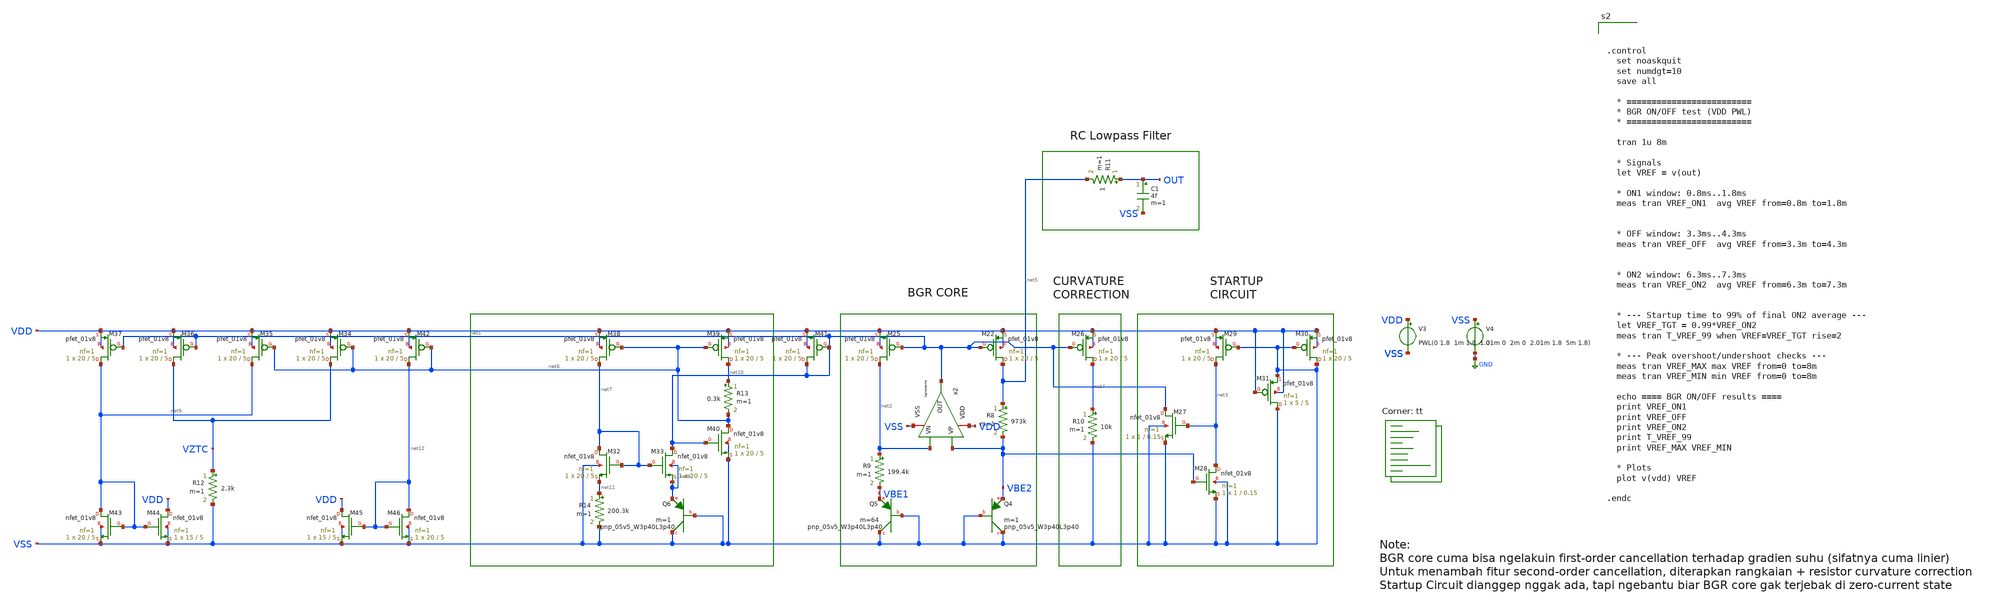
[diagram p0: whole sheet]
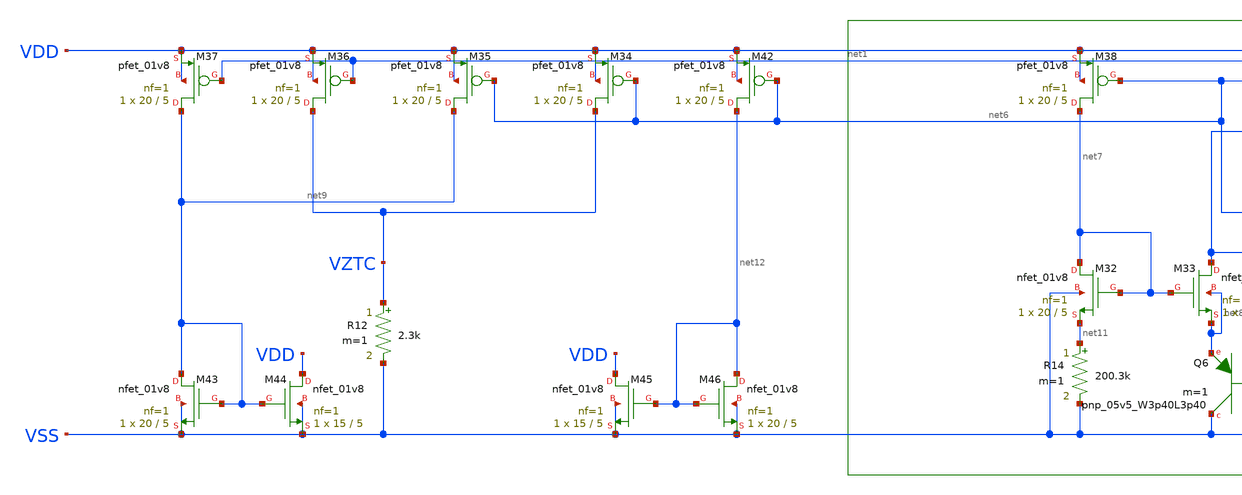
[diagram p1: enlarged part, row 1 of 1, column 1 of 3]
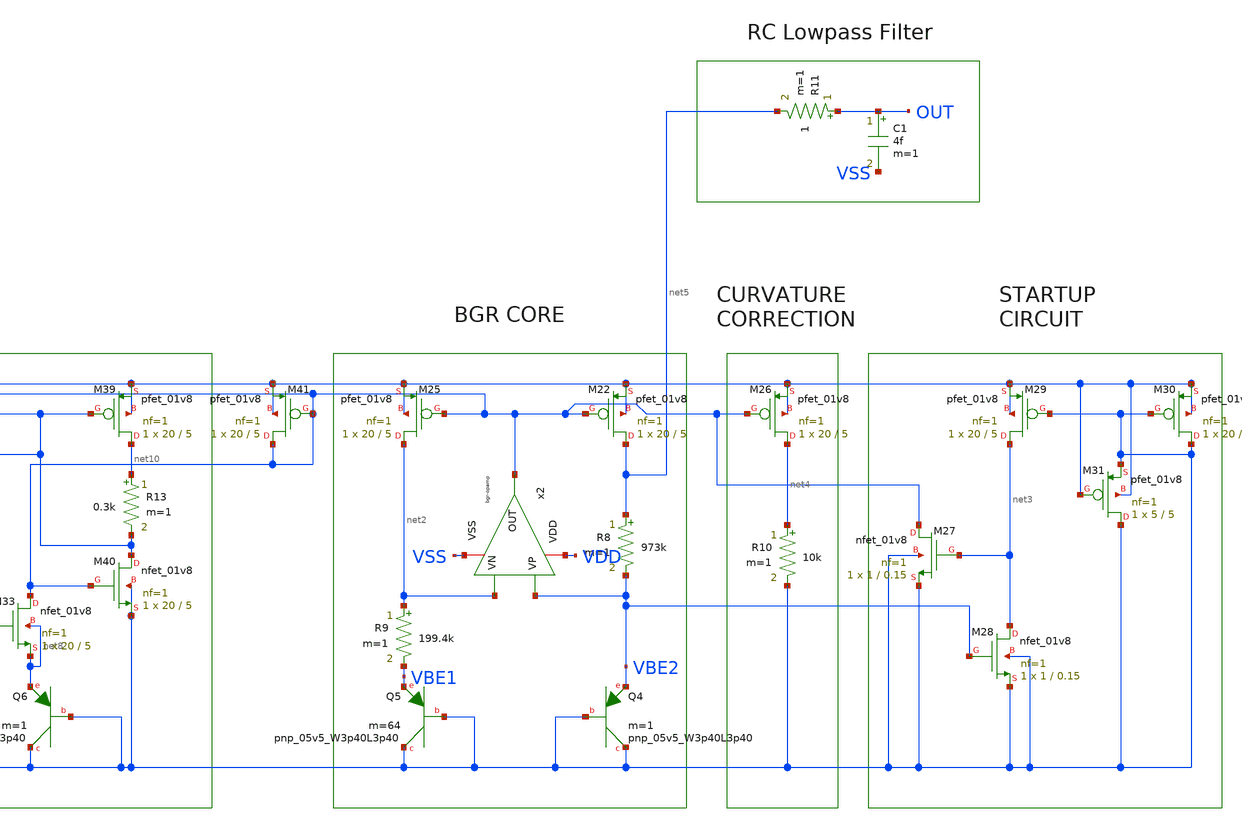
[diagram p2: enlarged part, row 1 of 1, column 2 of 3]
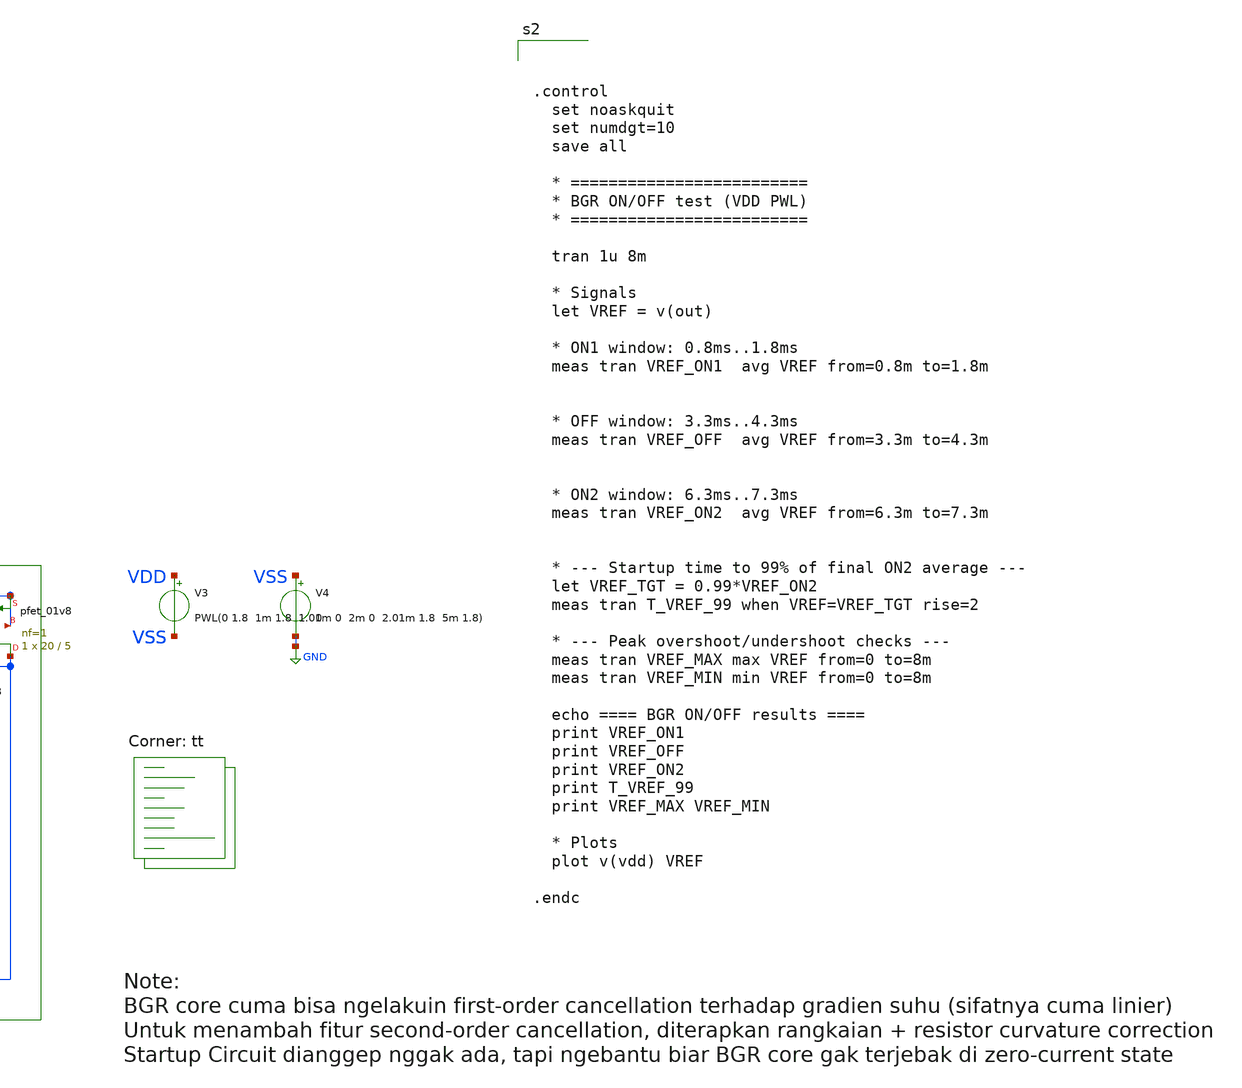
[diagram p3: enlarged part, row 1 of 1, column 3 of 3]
** sch_path: bandgap/bgr-final/tb_bgr-on-off.sch
**.subckt tb_bgr-on-off
V3 VDD VSS PWL(0 1.8 1m 1.8 1.01m 0 2m 0 2.01m 1.8 5m 1.8)
V4 VSS GND 0
x2 VDD net1 VBE2 net2 VSS bgr-opamp
XM22 net5 net1 VDD VDD sky130_fd_pr__pfet_01v8 L=5 W=20 nf=1 ad='int((nf+1)/2) * W/nf * 0.29' as='int((nf+2)/2) * W/nf * 0.29'
+ pd='2*int((nf+1)/2) * (W/nf + 0.29)' ps='2*int((nf+2)/2) * (W/nf + 0.29)' nrd='0.29 / W' nrs='0.29 / W'
+ sa=0 sb=0 sd=0 mult=1 m=1
XM25 net2 net1 VDD VDD sky130_fd_pr__pfet_01v8 L=5 W=20 nf=1 ad='int((nf+1)/2) * W/nf * 0.29' as='int((nf+2)/2) * W/nf * 0.29'
+ pd='2*int((nf+1)/2) * (W/nf + 0.29)' ps='2*int((nf+2)/2) * (W/nf + 0.29)' nrd='0.29 / W' nrs='0.29 / W'
+ sa=0 sb=0 sd=0 mult=1 m=1
R8 net5 VBE2 973k m=1
R9 net2 VBE1 199.4k m=1
XQ4 VSS VSS VBE2 sky130_fd_pr__pnp_05v5_W3p40L3p40 m=1
XQ5 VSS VSS VBE1 sky130_fd_pr__pnp_05v5_W3p40L3p40 m=64
XM26 net4 net1 VDD VDD sky130_fd_pr__pfet_01v8 L=5 W=20 nf=1 ad='int((nf+1)/2) * W/nf * 0.29' as='int((nf+2)/2) * W/nf * 0.29'
+ pd='2*int((nf+1)/2) * (W/nf + 0.29)' ps='2*int((nf+2)/2) * (W/nf + 0.29)' nrd='0.29 / W' nrs='0.29 / W'
+ sa=0 sb=0 sd=0 mult=1 m=1
R10 net4 VSS 10k m=1
XM27 net1 net3 VSS VSS sky130_fd_pr__nfet_01v8 L=0.15 W=1 nf=1 ad='int((nf+1)/2) * W/nf * 0.29' as='int((nf+2)/2) * W/nf * 0.29'
+ pd='2*int((nf+1)/2) * (W/nf + 0.29)' ps='2*int((nf+2)/2) * (W/nf + 0.29)' nrd='0.29 / W' nrs='0.29 / W'
+ sa=0 sb=0 sd=0 mult=1 m=1
XM28 net3 VBE2 VSS VSS sky130_fd_pr__nfet_01v8 L=0.15 W=1 nf=1 ad='int((nf+1)/2) * W/nf * 0.29' as='int((nf+2)/2) * W/nf * 0.29'
+ pd='2*int((nf+1)/2) * (W/nf + 0.29)' ps='2*int((nf+2)/2) * (W/nf + 0.29)' nrd='0.29 / W' nrs='0.29 / W'
+ sa=0 sb=0 sd=0 mult=1 m=1
XM29 net3 VSS VDD VDD sky130_fd_pr__pfet_01v8 L=5 W=20 nf=1 ad='int((nf+1)/2) * W/nf * 0.29' as='int((nf+2)/2) * W/nf * 0.29'
+ pd='2*int((nf+1)/2) * (W/nf + 0.29)' ps='2*int((nf+2)/2) * (W/nf + 0.29)' nrd='0.29 / W' nrs='0.29 / W'
+ sa=0 sb=0 sd=0 mult=1 m=1
XM30 VSS VSS VDD VDD sky130_fd_pr__pfet_01v8 L=5 W=20 nf=1 ad='int((nf+1)/2) * W/nf * 0.29' as='int((nf+2)/2) * W/nf * 0.29'
+ pd='2*int((nf+1)/2) * (W/nf + 0.29)' ps='2*int((nf+2)/2) * (W/nf + 0.29)' nrd='0.29 / W' nrs='0.29 / W'
+ sa=0 sb=0 sd=0 mult=1 m=1
XM31 VSS VDD VSS VDD sky130_fd_pr__pfet_01v8 L=5 W=5 nf=1 ad='int((nf+1)/2) * W/nf * 0.29' as='int((nf+2)/2) * W/nf * 0.29'
+ pd='2*int((nf+1)/2) * (W/nf + 0.29)' ps='2*int((nf+2)/2) * (W/nf + 0.29)' nrd='0.29 / W' nrs='0.29 / W'
+ sa=0 sb=0 sd=0 mult=1 m=1
C1 OUT VSS 4f m=1
R11 OUT net5 1 m=1
XM32 net7 net7 net11 VSS sky130_fd_pr__nfet_01v8 L=5 W=20 nf=1 ad='int((nf+1)/2) * W/nf * 0.29' as='int((nf+2)/2) * W/nf * 0.29'
+ pd='2*int((nf+1)/2) * (W/nf + 0.29)' ps='2*int((nf+2)/2) * (W/nf + 0.29)' nrd='0.29 / W' nrs='0.29 / W'
+ sa=0 sb=0 sd=0 mult=1 m=1
XM33 net1 net7 net8 net8 sky130_fd_pr__nfet_01v8 L=5 W=20 nf=1 ad='int((nf+1)/2) * W/nf * 0.29' as='int((nf+2)/2) * W/nf * 0.29'
+ pd='2*int((nf+1)/2) * (W/nf + 0.29)' ps='2*int((nf+2)/2) * (W/nf + 0.29)' nrd='0.29 / W' nrs='0.29 / W'
+ sa=0 sb=0 sd=0 mult=1 m=1
XQ6 VSS VSS net8 sky130_fd_pr__pnp_05v5_W3p40L3p40 m=1
XM34 VZTC net6 VDD VDD sky130_fd_pr__pfet_01v8 L=5 W=20 nf=1 ad='int((nf+1)/2) * W/nf * 0.29' as='int((nf+2)/2) * W/nf * 0.29'
+ pd='2*int((nf+1)/2) * (W/nf + 0.29)' ps='2*int((nf+2)/2) * (W/nf + 0.29)' nrd='0.29 / W' nrs='0.29 / W'
+ sa=0 sb=0 sd=0 mult=1 m=1
XM35 net9 net6 VDD VDD sky130_fd_pr__pfet_01v8 L=5 W=20 nf=1 ad='int((nf+1)/2) * W/nf * 0.29' as='int((nf+2)/2) * W/nf * 0.29'
+ pd='2*int((nf+1)/2) * (W/nf + 0.29)' ps='2*int((nf+2)/2) * (W/nf + 0.29)' nrd='0.29 / W' nrs='0.29 / W'
+ sa=0 sb=0 sd=0 mult=1 m=1
XM36 VZTC net1 VDD VDD sky130_fd_pr__pfet_01v8 L=5 W=20 nf=1 ad='int((nf+1)/2) * W/nf * 0.29' as='int((nf+2)/2) * W/nf * 0.29'
+ pd='2*int((nf+1)/2) * (W/nf + 0.29)' ps='2*int((nf+2)/2) * (W/nf + 0.29)' nrd='0.29 / W' nrs='0.29 / W'
+ sa=0 sb=0 sd=0 mult=1 m=1
XM37 net9 net1 VDD VDD sky130_fd_pr__pfet_01v8 L=5 W=20 nf=1 ad='int((nf+1)/2) * W/nf * 0.29' as='int((nf+2)/2) * W/nf * 0.29'
+ pd='2*int((nf+1)/2) * (W/nf + 0.29)' ps='2*int((nf+2)/2) * (W/nf + 0.29)' nrd='0.29 / W' nrs='0.29 / W'
+ sa=0 sb=0 sd=0 mult=1 m=1
R12 VZTC VSS 2.3k m=1
XM38 net7 net6 VDD VDD sky130_fd_pr__pfet_01v8 L=5 W=20 nf=1 ad='int((nf+1)/2) * W/nf * 0.29' as='int((nf+2)/2) * W/nf * 0.29'
+ pd='2*int((nf+1)/2) * (W/nf + 0.29)' ps='2*int((nf+2)/2) * (W/nf + 0.29)' nrd='0.29 / W' nrs='0.29 / W'
+ sa=0 sb=0 sd=0 mult=1 m=1
XM39 net10 net6 VDD VDD sky130_fd_pr__pfet_01v8 L=5 W=20 nf=1 ad='int((nf+1)/2) * W/nf * 0.29' as='int((nf+2)/2) * W/nf * 0.29'
+ pd='2*int((nf+1)/2) * (W/nf + 0.29)' ps='2*int((nf+2)/2) * (W/nf + 0.29)' nrd='0.29 / W' nrs='0.29 / W'
+ sa=0 sb=0 sd=0 mult=1 m=1
R13 net10 net6 0.3k m=1
XM40 net6 net1 VSS VSS sky130_fd_pr__nfet_01v8 L=5 W=20 nf=1 ad='int((nf+1)/2) * W/nf * 0.29' as='int((nf+2)/2) * W/nf * 0.29'
+ pd='2*int((nf+1)/2) * (W/nf + 0.29)' ps='2*int((nf+2)/2) * (W/nf + 0.29)' nrd='0.29 / W' nrs='0.29 / W'
+ sa=0 sb=0 sd=0 mult=1 m=1
XM41 net1 net1 VDD VDD sky130_fd_pr__pfet_01v8 L=5 W=20 nf=1 ad='int((nf+1)/2) * W/nf * 0.29' as='int((nf+2)/2) * W/nf * 0.29'
+ pd='2*int((nf+1)/2) * (W/nf + 0.29)' ps='2*int((nf+2)/2) * (W/nf + 0.29)' nrd='0.29 / W' nrs='0.29 / W'
+ sa=0 sb=0 sd=0 mult=1 m=1
R14 net11 VSS 200.3k m=1
XM42 net12 net6 VDD VDD sky130_fd_pr__pfet_01v8 L=5 W=20 nf=1 ad='int((nf+1)/2) * W/nf * 0.29' as='int((nf+2)/2) * W/nf * 0.29'
+ pd='2*int((nf+1)/2) * (W/nf + 0.29)' ps='2*int((nf+2)/2) * (W/nf + 0.29)' nrd='0.29 / W' nrs='0.29 / W'
+ sa=0 sb=0 sd=0 mult=1 m=1
XM43 net9 net9 VSS VSS sky130_fd_pr__nfet_01v8 L=5 W=20 nf=1 ad='int((nf+1)/2) * W/nf * 0.29' as='int((nf+2)/2) * W/nf * 0.29'
+ pd='2*int((nf+1)/2) * (W/nf + 0.29)' ps='2*int((nf+2)/2) * (W/nf + 0.29)' nrd='0.29 / W' nrs='0.29 / W'
+ sa=0 sb=0 sd=0 mult=1 m=1
XM44 VDD net9 VSS VSS sky130_fd_pr__nfet_01v8 L=5 W=15 nf=1 ad='int((nf+1)/2) * W/nf * 0.29' as='int((nf+2)/2) * W/nf * 0.29'
+ pd='2*int((nf+1)/2) * (W/nf + 0.29)' ps='2*int((nf+2)/2) * (W/nf + 0.29)' nrd='0.29 / W' nrs='0.29 / W'
+ sa=0 sb=0 sd=0 mult=1 m=1
XM45 VDD net12 VSS VSS sky130_fd_pr__nfet_01v8 L=5 W=15 nf=1 ad='int((nf+1)/2) * W/nf * 0.29' as='int((nf+2)/2) * W/nf * 0.29'
+ pd='2*int((nf+1)/2) * (W/nf + 0.29)' ps='2*int((nf+2)/2) * (W/nf + 0.29)' nrd='0.29 / W' nrs='0.29 / W'
+ sa=0 sb=0 sd=0 mult=1 m=1
XM46 net12 net12 VSS VSS sky130_fd_pr__nfet_01v8 L=5 W=20 nf=1 ad='int((nf+1)/2) * W/nf * 0.29' as='int((nf+2)/2) * W/nf * 0.29'
+ pd='2*int((nf+1)/2) * (W/nf + 0.29)' ps='2*int((nf+2)/2) * (W/nf + 0.29)' nrd='0.29 / W' nrs='0.29 / W'
+ sa=0 sb=0 sd=0 mult=1 m=1
**** begin user architecture code
.lib $::SKYWATER_MODELS/sky130.lib.spice tt



.control
  set noaskquit
  set numdgt=10
  save all

  * =========================
  * BGR ON/OFF test (VDD PWL)
  * =========================

  tran 1u 8m

  * Signals
  let VREF = v(out)

  * ON1 window: 0.8ms..1.8ms
  meas tran VREF_ON1  avg VREF from=0.8m to=1.8m


  * OFF window: 3.3ms..4.3ms
  meas tran VREF_OFF  avg VREF from=3.3m to=4.3m


  * ON2 window: 6.3ms..7.3ms
  meas tran VREF_ON2  avg VREF from=6.3m to=7.3m


  * --- Startup time to 99% of final ON2 average ---
  let VREF_TGT = 0.99*VREF_ON2
  meas tran T_VREF_99 when VREF=VREF_TGT rise=2

  * --- Peak overshoot/undershoot checks ---
  meas tran VREF_MAX max VREF from=0 to=8m
  meas tran VREF_MIN min VREF from=0 to=8m

  echo ==== BGR ON/OFF results ====
  print VREF_ON1
  print VREF_OFF
  print VREF_ON2
  print T_VREF_99
  print VREF_MAX VREF_MIN

  * Plots
  plot v(vdd) VREF

.endc


**** end user architecture code
**.ends

* expanding   symbol:  afe-icdec-teknofest-2026/bandgap/bgr-opamp/bgr-opamp.sym # of pins=5
** sym_path: bandgap/bgr-opamp/bgr-opamp.sym
** sch_path: bandgap/bgr-opamp/bgr-opamp.sch
.subckt bgr-opamp VDD OUT VP VN VSS
*.iopin VSS
*.iopin VDD
*.ipin VP
*.ipin VN
*.opin OUT
XM1 net1 VP net3 VSS sky130_fd_pr__nfet_01v8 L=0.3 W=2.5 nf=2 ad='int((nf+1)/2) * W/nf * 0.29' as='int((nf+2)/2) * W/nf * 0.29'
+ pd='2*int((nf+1)/2) * (W/nf + 0.29)' ps='2*int((nf+2)/2) * (W/nf + 0.29)' nrd='0.29 / W' nrs='0.29 / W'
+ sa=0 sb=0 sd=0 mult=1 m=1
XM2 net2 VN net3 VSS sky130_fd_pr__nfet_01v8 L=0.3 W=2.5 nf=2 ad='int((nf+1)/2) * W/nf * 0.29' as='int((nf+2)/2) * W/nf * 0.29'
+ pd='2*int((nf+1)/2) * (W/nf + 0.29)' ps='2*int((nf+2)/2) * (W/nf + 0.29)' nrd='0.29 / W' nrs='0.29 / W'
+ sa=0 sb=0 sd=0 mult=1 m=1
XM4 net2 net1 VDD VDD sky130_fd_pr__pfet_01v8 L=1.25 W=10.8 nf=4 ad='int((nf+1)/2) * W/nf * 0.29' as='int((nf+2)/2) * W/nf * 0.29'
+ pd='2*int((nf+1)/2) * (W/nf + 0.29)' ps='2*int((nf+2)/2) * (W/nf + 0.29)' nrd='0.29 / W' nrs='0.29 / W'
+ sa=0 sb=0 sd=0 mult=1 m=1
XM3 net1 net1 VDD VDD sky130_fd_pr__pfet_01v8 L=1.25 W=10.8 nf=4 ad='int((nf+1)/2) * W/nf * 0.29' as='int((nf+2)/2) * W/nf * 0.29'
+ pd='2*int((nf+1)/2) * (W/nf + 0.29)' ps='2*int((nf+2)/2) * (W/nf + 0.29)' nrd='0.29 / W' nrs='0.29 / W'
+ sa=0 sb=0 sd=0 mult=1 m=1
XM5 net3 net4 VSS VSS sky130_fd_pr__nfet_01v8 L=1.25 W=3.4 nf=1 ad='int((nf+1)/2) * W/nf * 0.29' as='int((nf+2)/2) * W/nf * 0.29'
+ pd='2*int((nf+1)/2) * (W/nf + 0.29)' ps='2*int((nf+2)/2) * (W/nf + 0.29)' nrd='0.29 / W' nrs='0.29 / W'
+ sa=0 sb=0 sd=0 mult=1 m=1
XM9 net4 net5 net10 VSS sky130_fd_pr__nfet_01v8 L=1.25 W=3.4 nf=1 ad='int((nf+1)/2) * W/nf * 0.29' as='int((nf+2)/2) * W/nf * 0.29'
+ pd='2*int((nf+1)/2) * (W/nf + 0.29)' ps='2*int((nf+2)/2) * (W/nf + 0.29)' nrd='0.29 / W' nrs='0.29 / W'
+ sa=0 sb=0 sd=0 mult=1 m=1
XM8 net4 net4 VDD VDD sky130_fd_pr__pfet_01v8 L=1.25 W=10.8 nf=4 ad='int((nf+1)/2) * W/nf * 0.29' as='int((nf+2)/2) * W/nf * 0.29'
+ pd='2*int((nf+1)/2) * (W/nf + 0.29)' ps='2*int((nf+2)/2) * (W/nf + 0.29)' nrd='0.29 / W' nrs='0.29 / W'
+ sa=0 sb=0 sd=0 mult=1 m=1
XM11 net5 net4 VDD VDD sky130_fd_pr__pfet_01v8 L=1.25 W=10.8 nf=4 ad='int((nf+1)/2) * W/nf * 0.29' as='int((nf+2)/2) * W/nf * 0.29'
+ pd='2*int((nf+1)/2) * (W/nf + 0.29)' ps='2*int((nf+2)/2) * (W/nf + 0.29)' nrd='0.29 / W' nrs='0.29 / W'
+ sa=0 sb=0 sd=0 mult=1 m=1
XM10 net5 net5 VSS VSS sky130_fd_pr__nfet_01v8 L=1.25 W=3.4 nf=1 ad='int((nf+1)/2) * W/nf * 0.29' as='int((nf+2)/2) * W/nf * 0.29'
+ pd='2*int((nf+1)/2) * (W/nf + 0.29)' ps='2*int((nf+2)/2) * (W/nf + 0.29)' nrd='0.29 / W' nrs='0.29 / W'
+ sa=0 sb=0 sd=0 mult=1 m=1
XM6 OUT net2 VDD VDD sky130_fd_pr__pfet_01v8 L=1.25 W=110 nf=32 ad='int((nf+1)/2) * W/nf * 0.29' as='int((nf+2)/2) * W/nf * 0.29'
+ pd='2*int((nf+1)/2) * (W/nf + 0.29)' ps='2*int((nf+2)/2) * (W/nf + 0.29)' nrd='0.29 / W' nrs='0.29 / W'
+ sa=0 sb=0 sd=0 mult=1 m=1
XM7 OUT net4 VSS VSS sky130_fd_pr__nfet_01v8 L=1.25 W=12 nf=4 ad='int((nf+1)/2) * W/nf * 0.29' as='int((nf+2)/2) * W/nf * 0.29'
+ pd='2*int((nf+1)/2) * (W/nf + 0.29)' ps='2*int((nf+2)/2) * (W/nf + 0.29)' nrd='0.29 / W' nrs='0.29 / W'
+ sa=0 sb=0 sd=0 mult=1 m=1
XC2 OUT net2 sky130_fd_pr__cap_mim_m3_1 W=15 L=15 MF=4 m=4
XM12 net4 net4 net5 VSS sky130_fd_pr__nfet_01v8 L=0.15 W=0.85 nf=1 ad='int((nf+1)/2) * W/nf * 0.29' as='int((nf+2)/2) * W/nf * 0.29'
+ pd='2*int((nf+1)/2) * (W/nf + 0.29)' ps='2*int((nf+2)/2) * (W/nf + 0.29)' nrd='0.29 / W' nrs='0.29 / W'
+ sa=0 sb=0 sd=0 mult=1 m=1
XR2 net6 net10 VSS sky130_fd_pr__res_high_po_1p41 L=3.235 mult=1 m=1
XR3 net8 net6 VSS sky130_fd_pr__res_high_po_1p41 L=3.235 mult=1 m=1
XR4 net7 net8 VSS sky130_fd_pr__res_high_po_1p41 L=3.235 mult=1 m=1
XR5 net9 net7 VSS sky130_fd_pr__res_high_po_1p41 L=3.235 mult=1 m=1
XR6 VSS net9 VSS sky130_fd_pr__res_high_po_1p41 L=3.235 mult=1 m=1
.ends

.GLOBAL GND
.end
